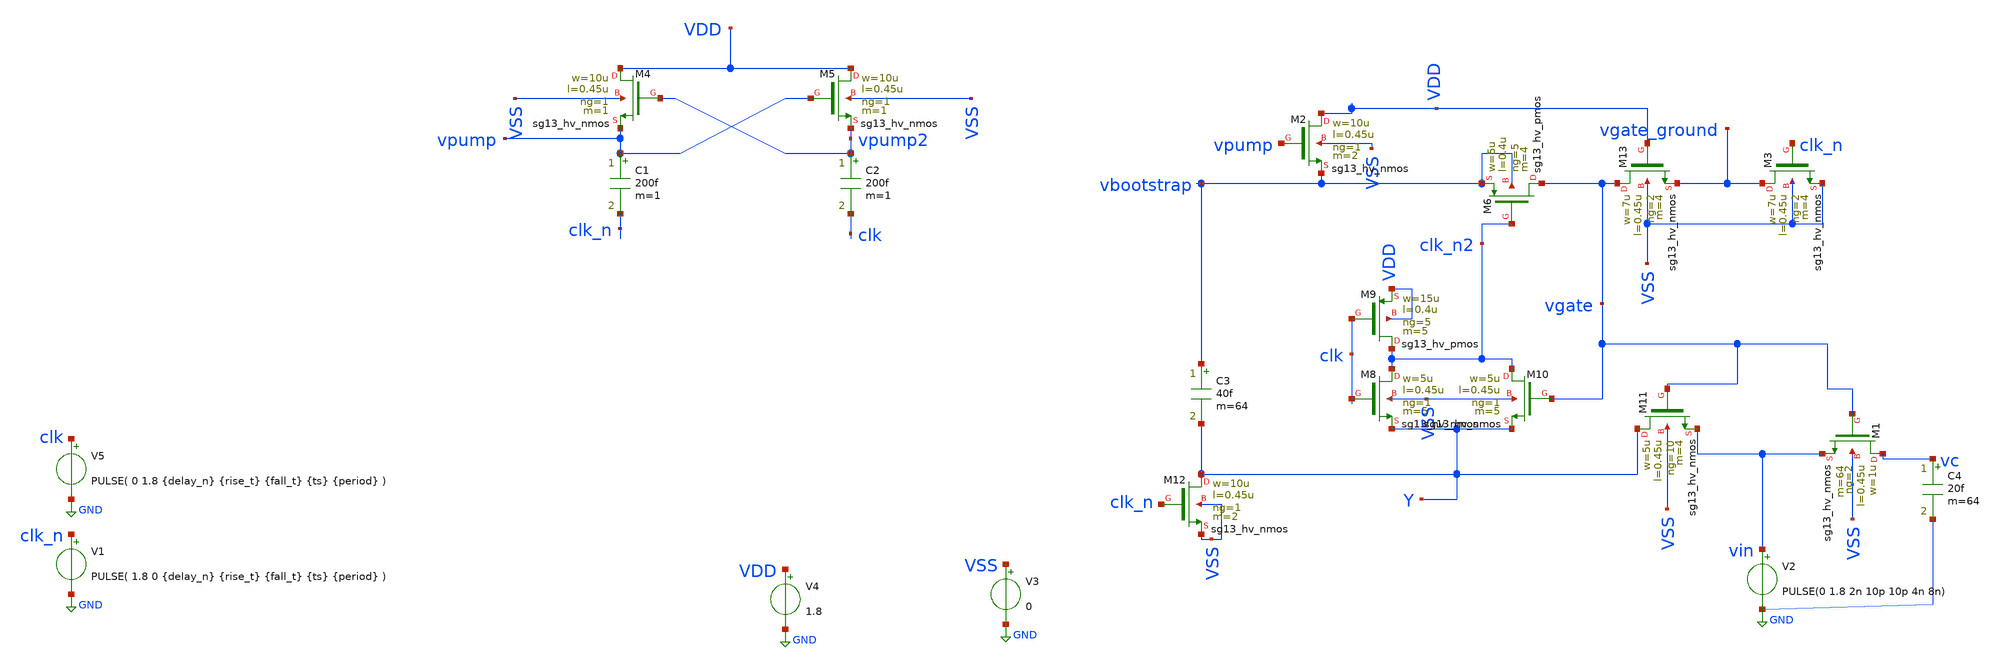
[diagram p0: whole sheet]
** sch_path: xschem/bootstrap/tb_bootstrap_pulse.sch
**.subckt tb_bootstrap_pulse
V2 vin GND PULSE(0 1.8 2n 10p 10p 4n 8n)
V4 VDD GND 1.8
C1 vpump clk_n 200f m=1
C2 vpump2 clk 200f m=1
XM6 vgate clk_n2 vbootstrap vbootstrap sg13_hv_pmos w=5u l=0.4u ng=5 m=4 mm_ok=1
XM8 clk_n2 clk Y VSS sg13_hv_nmos w=5u l=0.45u ng=1 m=5 mm_ok=1
XM9 clk_n2 clk VDD VDD sg13_hv_pmos w=15u l=0.4u ng=5 m=5 mm_ok=1
XM10 clk_n2 vgate Y VSS sg13_hv_nmos w=5u l=0.45u ng=1 m=5 mm_ok=1
XM11 Y vgate vin VSS sg13_hv_nmos w=5u l=0.45u ng=10 m=4 mm_ok=1
C3 vbootstrap Y 40f m=64
XM12 Y clk_n VSS VSS sg13_hv_nmos w=10u l=0.45u ng=1 m=2 mm_ok=1
XM13 vgate VDD vgate_ground VSS sg13_hv_nmos w=7u l=0.45u ng=2 m=4 mm_ok=1
XM3 vgate_ground clk_n VSS VSS sg13_hv_nmos w=7u l=0.45u ng=2 m=4 mm_ok=1
XM4 VDD vpump2 vpump VSS sg13_hv_nmos w=10u l=0.45u ng=1 m=1 mm_ok=1
XM5 VDD vpump vpump2 VSS sg13_hv_nmos w=10u l=0.45u ng=1 m=1 mm_ok=1
XM1 vc vgate vin VSS sg13_hv_nmos w=1u l=0.45u ng=2 m=64 mm_ok=1
V1 clk_n GND PULSE( 1.8 0 {delay_n} {rise_t} {fall_t} {ts} {period} )
V5 clk GND PULSE( 0 1.8 {delay_n} {rise_t} {fall_t} {ts} {period} )
C4 vc GND 20f m=64
V3 VSS GND 0
XM2 VDD vpump vbootstrap VSS sg13_hv_nmos w=10u l=0.45u ng=1 m=2 mm_ok=1
**** begin user architecture code


.param temp=27
.param ts=2n
.param period = 3*ts
.param wp = 1.5u
.param a = 1.8
.param wn = 0.5u
.param rise_t = period*0.01
.param fall_t = period*0.01
.param delay_n = 0
.param delay_s = 0
.param delay_2 = 0
.param delay_1 = 0
.options savecurrents klu method=gear reltol=1e-2 abstol=1e-15 gmin=1e-10
.control

* Transient Analysis
tran 1p 40n

plot clk clk_n vpump vpump2
plot vin vgate vc
plot vbootstrap vgate_ground  vgate Y clk clk_n clk_n2
.endc




** IHP models
.lib cornerMOSlv.lib mos_tt
.lib cornerMOShv.lib mos_tt
.lib cornerHBT.lib hbt_typ
.lib cornerRES.lib res_typ
.include /foss/pdks/ihp-sg13g2/libs.ref/sg13g2_stdcell/spice/sg13g2_stdcell.spice


**** end user architecture code
**.ends
.GLOBAL GND
.end
